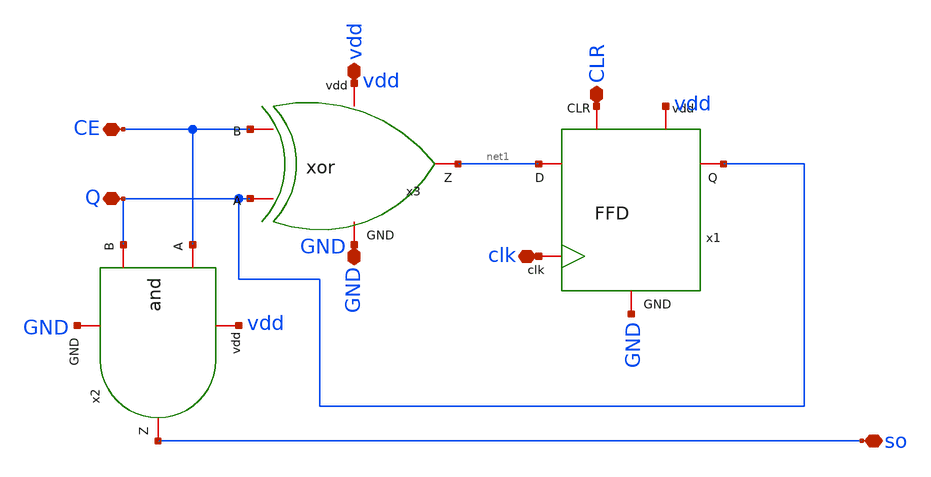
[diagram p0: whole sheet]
** sch_path: contador_1bit/count1b.sch
**.subckt count1b Q CLR clk so CE GND vdd
*.iopin Q
*.iopin CLR
*.iopin clk
*.iopin so
*.iopin CE
*.iopin GND
*.iopin vdd
x1 vdd GND CLR Q net1 clk FFD
x2 vdd CE so Q GND and
x3 vdd Q CE net1 GND xor
**.ends
.end
